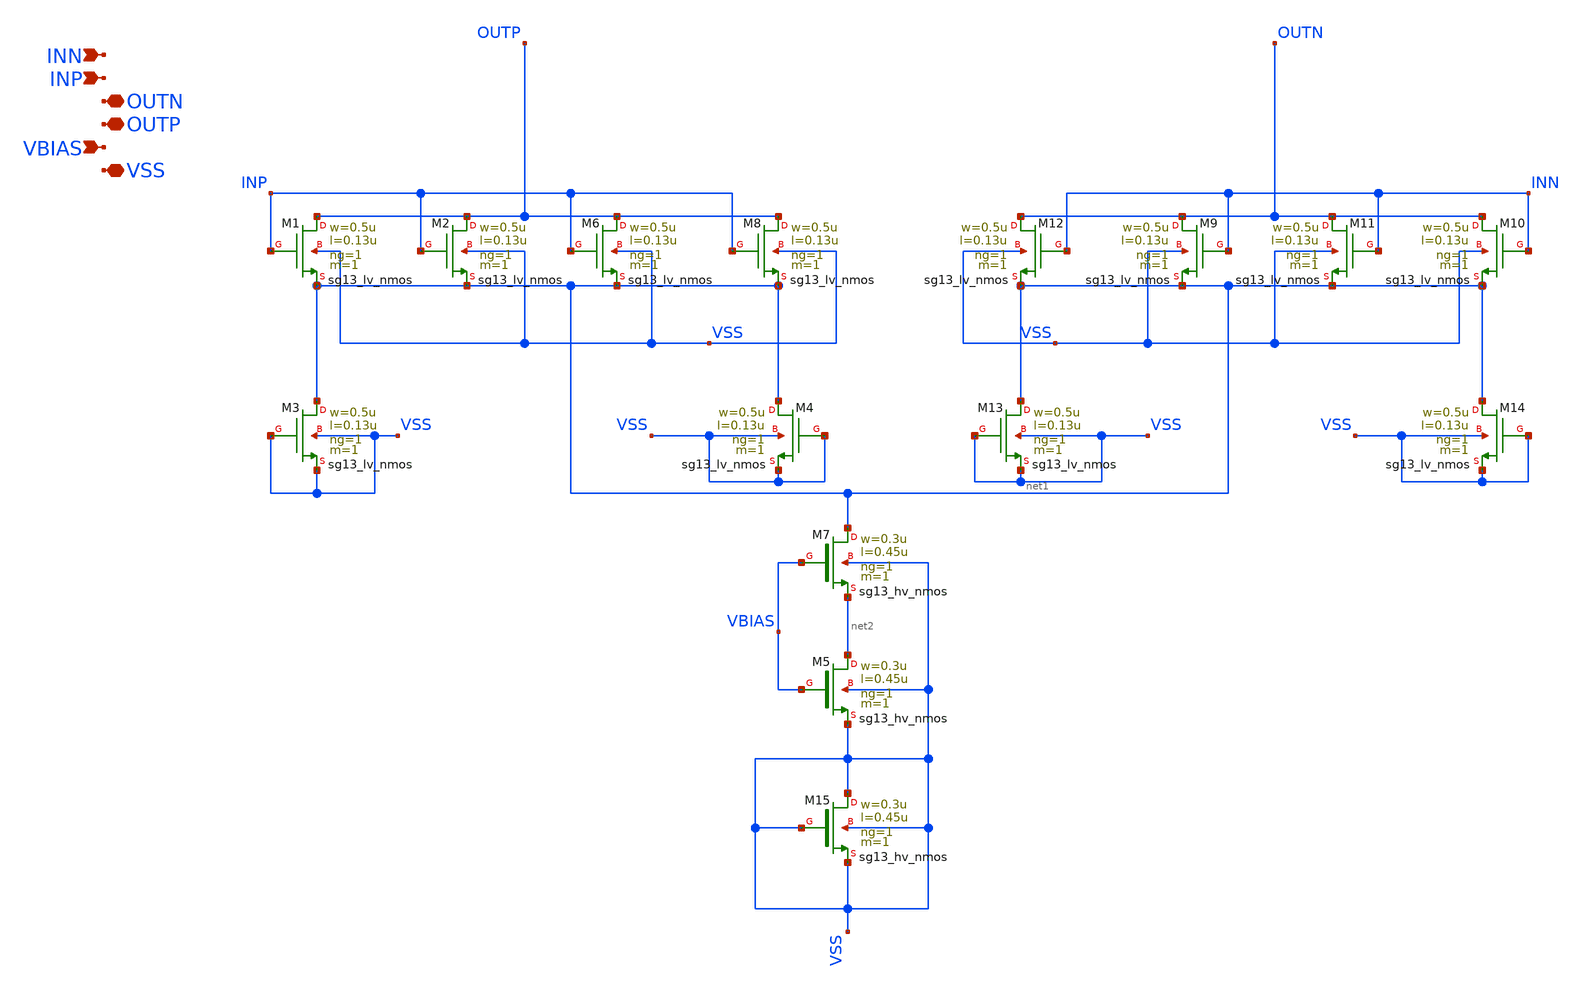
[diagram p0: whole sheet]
** sch_path: xschem/CS_Switch_1x.sch
**.subckt CS_Switch_1x VSS VBIAS OUTP OUTN INP INN
*.iopin VSS
*.ipin VBIAS
*.iopin OUTP
*.iopin OUTN
*.ipin INP
*.ipin INN
XM7 net1 VBIAS net2 VSS sg13_hv_nmos w=0.3u l=0.45u ng=1 m=1 mm_ok=1
XM5 net2 VBIAS VSS VSS sg13_hv_nmos w=0.3u l=0.45u ng=1 m=1 mm_ok=1
XM6 OUTP INP net1 VSS sg13_lv_nmos w=0.5u l=0.13u ng=1 m=1 mm_ok=1
XM1 OUTP INP net1 VSS sg13_lv_nmos w=0.5u l=0.13u ng=1 m=1 mm_ok=1
XM2 OUTP INP net1 VSS sg13_lv_nmos w=0.5u l=0.13u ng=1 m=1 mm_ok=1
XM8 OUTP INP net1 VSS sg13_lv_nmos w=0.5u l=0.13u ng=1 m=1 mm_ok=1
XM9 OUTN INN net1 VSS sg13_lv_nmos w=0.5u l=0.13u ng=1 m=1 mm_ok=1
XM10 OUTN INN net1 VSS sg13_lv_nmos w=0.5u l=0.13u ng=1 m=1 mm_ok=1
XM11 OUTN INN net1 VSS sg13_lv_nmos w=0.5u l=0.13u ng=1 m=1 mm_ok=1
XM12 OUTN INN net1 VSS sg13_lv_nmos w=0.5u l=0.13u ng=1 m=1 mm_ok=1
XM3 net1 VSS VSS VSS sg13_lv_nmos w=0.5u l=0.13u ng=1 m=1 mm_ok=1
XM4 net1 VSS VSS VSS sg13_lv_nmos w=0.5u l=0.13u ng=1 m=1 mm_ok=1
XM13 net1 VSS VSS VSS sg13_lv_nmos w=0.5u l=0.13u ng=1 m=1 mm_ok=1
XM14 net1 VSS VSS VSS sg13_lv_nmos w=0.5u l=0.13u ng=1 m=1 mm_ok=1
XM15 VSS VSS VSS VSS sg13_hv_nmos w=0.3u l=0.45u ng=1 m=1 mm_ok=1
**.ends
.end
